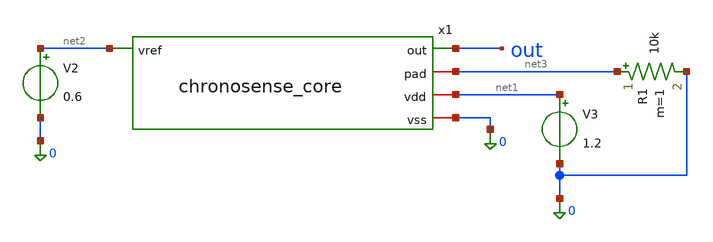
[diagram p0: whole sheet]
** sch_path: macros/heichips26_chronosense/testbenches/xschem/tb_core.sch
* macros/heichips26_chronosense/schematic/xschem/inv.sch:
* Copyright 2023 IHP PDK Authors
* Licensed under the Apache License, Version 2.0 (the "License");
**.subckt tb_core
x1 out net3 net2 net1 0 chronosense_core
V2 net2 0 0.6
V3 net1 0 1.2
R1 net3 0 10k m=1
**** begin user architecture code


.lib $PDKPATH/libs.tech/ngspice/models/cornerMOSlv.lib mos_tt
.lib $PDKPATH/libs.tech/ngspice/models/cornerRES.lib res_typ
.lib $PDKPATH/libs.tech/ngspice/models/cornerCAP.lib cap_typ
.param VDD=1.2 VREF=0.6 CT=15p
.ic v(x1.ctn)=0.5
.options method=gear reltol=1e-4 itl4=100
.tran 50p 3u
.control
run
meas tran t20  TRIG v(out) VAL=0.6 RISE=5 TARG v(out) VAL=0.6 RISE=25
let tper = t20/20
print tper
.endc


**** end user architecture code
**.ends

* expanding   symbol:  chronosense_core.sym # of pins=5
** sym_path: macros/heichips26_chronosense/schematic/xschem/chronosense_core.sym
** sch_path: macros/heichips26_chronosense/schematic/xschem/chronosense_core.sch
.subckt chronosense_core out pad vref vdd vss
*.iopin pad
*.ipin vref
*.opin out
*.iopin vss
*.iopin vdd
x1 vdd pad vref vss vg ota
x3 vdd sch schb vss inv
x4 vdd schb out vss inv
XXMRST ctn sch vss vss sg13_lv_nmos w=10u l=0.35u ng=1 m=1 mm_ok=1
XXMPASS pad vg vdd vdd sg13_lv_pmos w=5u l=1u ng=1 m=20 mm_ok=1
XXMMIR ctn vg vdd vdd sg13_lv_pmos w=5u l=1u ng=1 m=30 mm_ok=1
XCc vg vss cap_cmim w=18.25u l=18.25u m=4 mm_ok=1
XCT ctn vss cap_cmim w=25u l=25u m=16 mm_ok=1
x2 vdd sch vss ctn schmitt
.ends


* expanding   symbol:  ota.sym # of pins=5
** sym_path: macros/heichips26_chronosense/schematic/xschem/ota.sym
** sch_path: macros/heichips26_chronosense/schematic/xschem/ota.sch
.subckt ota vdd vin vip vss vout
*.opin vout
*.ipin vin
*.ipin vip
*.iopin vdd
*.iopin vss
XM1 vx vin vtail vss sg13_lv_nmos w=5u l=0.5u ng=1 m=4 mm_ok=1
XM3 vx vx vdd vdd sg13_lv_pmos w=5u l=1u ng=1 m=2 mm_ok=1
XM2 vout vip vtail vss sg13_lv_nmos w=5u l=0.5u ng=1 m=4 mm_ok=1
XM6 vb vb vss vss sg13_lv_nmos w=5u l=1u ng=1 m=2 mm_ok=1
XM5 vtail vb vss vss sg13_lv_nmos w=5u l=1u ng=1 m=2 mm_ok=1
XM4 vout vx vdd vdd sg13_lv_pmos w=5u l=1u ng=1 m=2 mm_ok=1
XR2 vdd vb vss rppd w=1u l=115.79u m=1 b=0 mm_ok=1
.ends


* expanding   symbol:  inv.sym # of pins=4
** sym_path: macros/heichips26_chronosense/schematic/xschem/inv.sym
** sch_path: macros/heichips26_chronosense/schematic/xschem/inv.sch
.subckt inv VDD IN OUT VSS
*.ipin IN
*.opin OUT
*.iopin VDD
*.iopin VSS
XM1 OUT IN VDD VDD sg13_lv_pmos w=2u l=0.35u ng=1 m=1 mm_ok=1
XM2 OUT IN VSS VSS sg13_lv_nmos w=1u l=0.35u ng=1 m=1 mm_ok=1
.ends


* expanding   symbol:  schmitt.sym # of pins=4
** sym_path: macros/heichips26_chronosense/schematic/xschem/schmitt.sym
** sch_path: macros/heichips26_chronosense/schematic/xschem/schmitt.sch
.subckt schmitt vdd out vss in
*.ipin in
*.iopin vdd
*.iopin vss
*.opin out
XM1 net2 in vss vss sg13_lv_nmos w=3u l=0.35u ng=1 m=1 mm_ok=1
XM2 net1 in vdd vdd sg13_lv_pmos w=6u l=0.35u ng=1 m=1 mm_ok=1
XM3 net3 in net2 vss sg13_lv_nmos w=3u l=0.35u ng=1 m=1 mm_ok=1
XM4 net2 net3 vdd vss sg13_lv_nmos w=3u l=0.35u ng=1 m=1 mm_ok=1
XM5 net3 in net1 vdd sg13_lv_pmos w=6u l=0.35u ng=1 m=1 mm_ok=1
XM6 net1 net3 vss vdd sg13_lv_pmos w=6u l=0.35u ng=1 m=1 mm_ok=1
x3 vdd net3 out vss inv
.ends

.end
